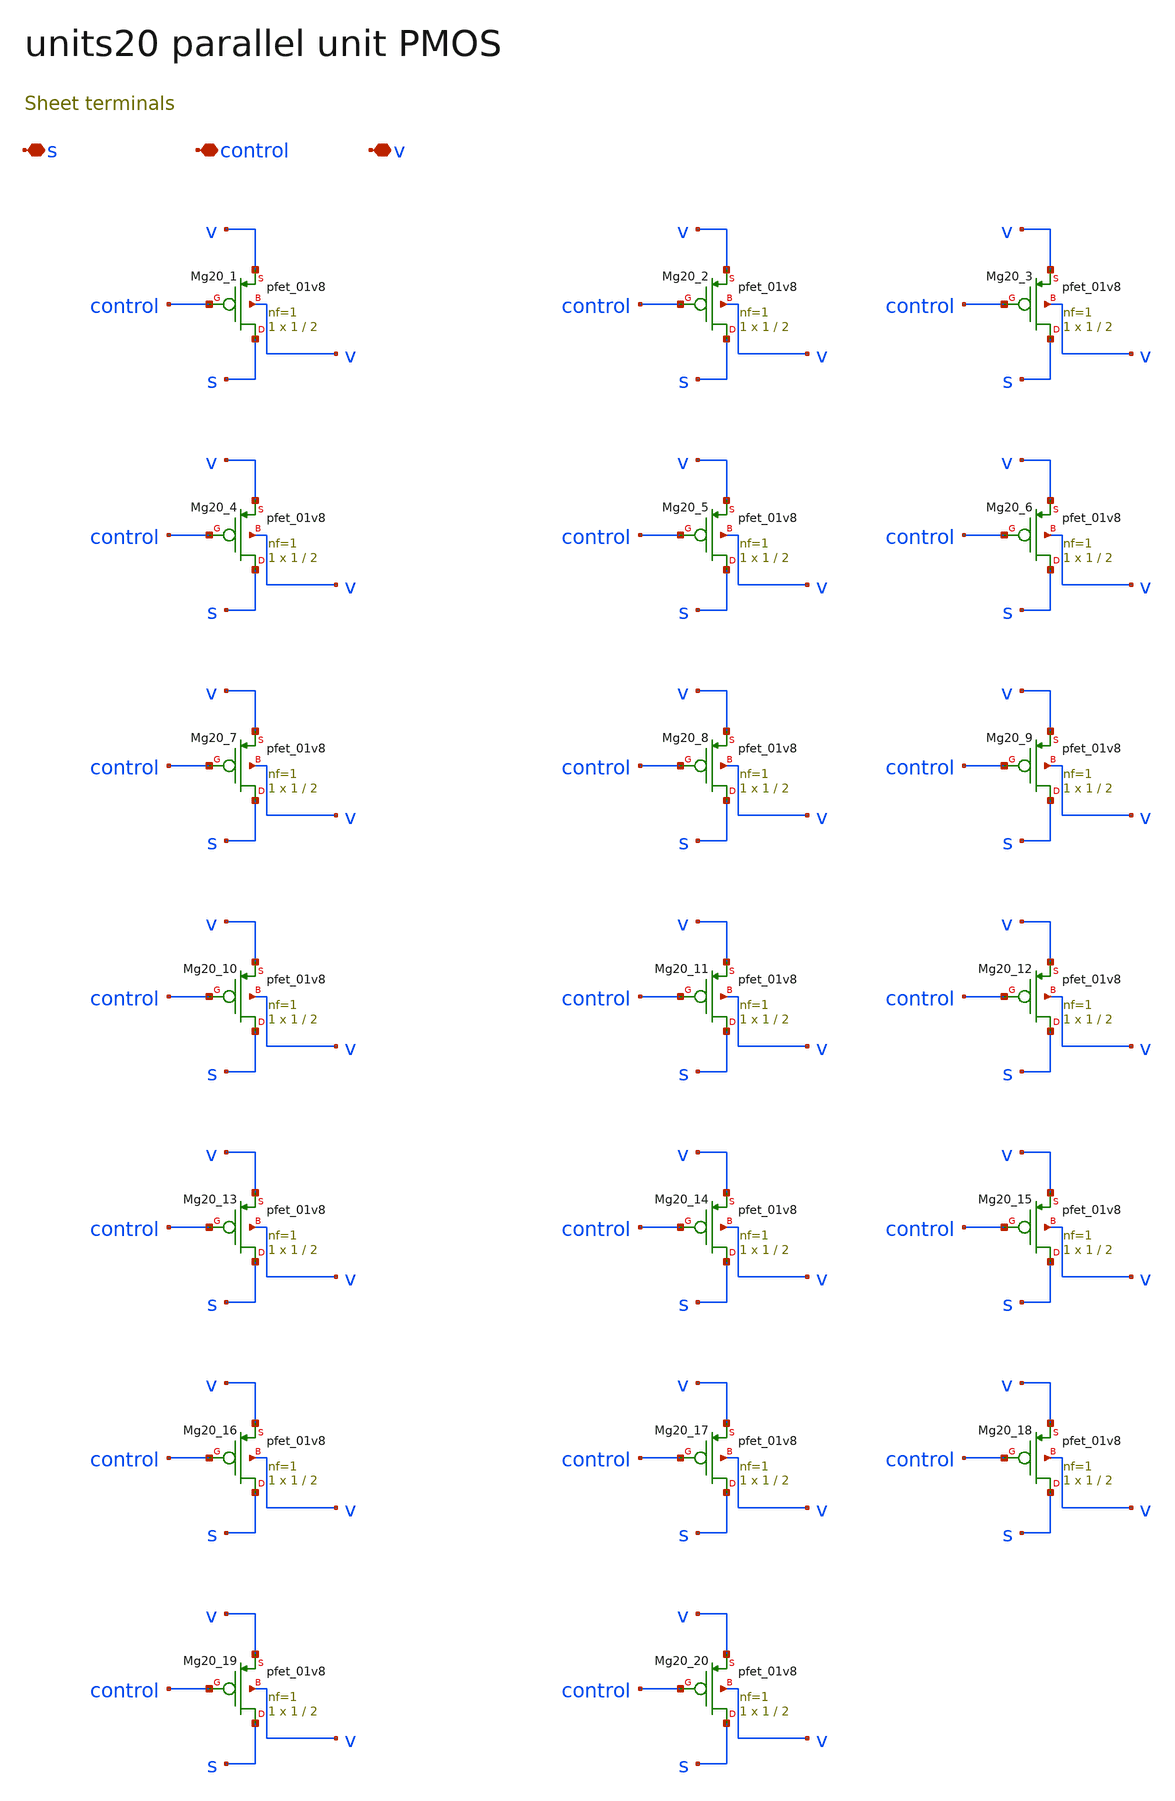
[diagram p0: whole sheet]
** sch_path: review/xschem/units20.sch
**.subckt units20 s control v
*.iopin s
*.iopin control
*.iopin v
XMg20_1 s control v v sky130_fd_pr__pfet_01v8 L=2 W=1 nf=1 ad='int((nf+1)/2) * W/nf * 0.29' as='int((nf+2)/2) * W/nf * 0.29'
+ pd='2*int((nf+1)/2) * (W/nf + 0.29)' ps='2*int((nf+2)/2) * (W/nf + 0.29)' nrd='0.29 / W' nrs='0.29 / W'
+ sa=0 sb=0 sd=0 mult=1 m=1
XMg20_2 s control v v sky130_fd_pr__pfet_01v8 L=2 W=1 nf=1 ad='int((nf+1)/2) * W/nf * 0.29' as='int((nf+2)/2) * W/nf * 0.29'
+ pd='2*int((nf+1)/2) * (W/nf + 0.29)' ps='2*int((nf+2)/2) * (W/nf + 0.29)' nrd='0.29 / W' nrs='0.29 / W'
+ sa=0 sb=0 sd=0 mult=1 m=1
XMg20_3 s control v v sky130_fd_pr__pfet_01v8 L=2 W=1 nf=1 ad='int((nf+1)/2) * W/nf * 0.29' as='int((nf+2)/2) * W/nf * 0.29'
+ pd='2*int((nf+1)/2) * (W/nf + 0.29)' ps='2*int((nf+2)/2) * (W/nf + 0.29)' nrd='0.29 / W' nrs='0.29 / W'
+ sa=0 sb=0 sd=0 mult=1 m=1
XMg20_4 s control v v sky130_fd_pr__pfet_01v8 L=2 W=1 nf=1 ad='int((nf+1)/2) * W/nf * 0.29' as='int((nf+2)/2) * W/nf * 0.29'
+ pd='2*int((nf+1)/2) * (W/nf + 0.29)' ps='2*int((nf+2)/2) * (W/nf + 0.29)' nrd='0.29 / W' nrs='0.29 / W'
+ sa=0 sb=0 sd=0 mult=1 m=1
XMg20_5 s control v v sky130_fd_pr__pfet_01v8 L=2 W=1 nf=1 ad='int((nf+1)/2) * W/nf * 0.29' as='int((nf+2)/2) * W/nf * 0.29'
+ pd='2*int((nf+1)/2) * (W/nf + 0.29)' ps='2*int((nf+2)/2) * (W/nf + 0.29)' nrd='0.29 / W' nrs='0.29 / W'
+ sa=0 sb=0 sd=0 mult=1 m=1
XMg20_6 s control v v sky130_fd_pr__pfet_01v8 L=2 W=1 nf=1 ad='int((nf+1)/2) * W/nf * 0.29' as='int((nf+2)/2) * W/nf * 0.29'
+ pd='2*int((nf+1)/2) * (W/nf + 0.29)' ps='2*int((nf+2)/2) * (W/nf + 0.29)' nrd='0.29 / W' nrs='0.29 / W'
+ sa=0 sb=0 sd=0 mult=1 m=1
XMg20_7 s control v v sky130_fd_pr__pfet_01v8 L=2 W=1 nf=1 ad='int((nf+1)/2) * W/nf * 0.29' as='int((nf+2)/2) * W/nf * 0.29'
+ pd='2*int((nf+1)/2) * (W/nf + 0.29)' ps='2*int((nf+2)/2) * (W/nf + 0.29)' nrd='0.29 / W' nrs='0.29 / W'
+ sa=0 sb=0 sd=0 mult=1 m=1
XMg20_8 s control v v sky130_fd_pr__pfet_01v8 L=2 W=1 nf=1 ad='int((nf+1)/2) * W/nf * 0.29' as='int((nf+2)/2) * W/nf * 0.29'
+ pd='2*int((nf+1)/2) * (W/nf + 0.29)' ps='2*int((nf+2)/2) * (W/nf + 0.29)' nrd='0.29 / W' nrs='0.29 / W'
+ sa=0 sb=0 sd=0 mult=1 m=1
XMg20_9 s control v v sky130_fd_pr__pfet_01v8 L=2 W=1 nf=1 ad='int((nf+1)/2) * W/nf * 0.29' as='int((nf+2)/2) * W/nf * 0.29'
+ pd='2*int((nf+1)/2) * (W/nf + 0.29)' ps='2*int((nf+2)/2) * (W/nf + 0.29)' nrd='0.29 / W' nrs='0.29 / W'
+ sa=0 sb=0 sd=0 mult=1 m=1
XMg20_10 s control v v sky130_fd_pr__pfet_01v8 L=2 W=1 nf=1 ad='int((nf+1)/2) * W/nf * 0.29' as='int((nf+2)/2) * W/nf * 0.29'
+ pd='2*int((nf+1)/2) * (W/nf + 0.29)' ps='2*int((nf+2)/2) * (W/nf + 0.29)' nrd='0.29 / W' nrs='0.29 / W'
+ sa=0 sb=0 sd=0 mult=1 m=1
XMg20_11 s control v v sky130_fd_pr__pfet_01v8 L=2 W=1 nf=1 ad='int((nf+1)/2) * W/nf * 0.29' as='int((nf+2)/2) * W/nf * 0.29'
+ pd='2*int((nf+1)/2) * (W/nf + 0.29)' ps='2*int((nf+2)/2) * (W/nf + 0.29)' nrd='0.29 / W' nrs='0.29 / W'
+ sa=0 sb=0 sd=0 mult=1 m=1
XMg20_12 s control v v sky130_fd_pr__pfet_01v8 L=2 W=1 nf=1 ad='int((nf+1)/2) * W/nf * 0.29' as='int((nf+2)/2) * W/nf * 0.29'
+ pd='2*int((nf+1)/2) * (W/nf + 0.29)' ps='2*int((nf+2)/2) * (W/nf + 0.29)' nrd='0.29 / W' nrs='0.29 / W'
+ sa=0 sb=0 sd=0 mult=1 m=1
XMg20_13 s control v v sky130_fd_pr__pfet_01v8 L=2 W=1 nf=1 ad='int((nf+1)/2) * W/nf * 0.29' as='int((nf+2)/2) * W/nf * 0.29'
+ pd='2*int((nf+1)/2) * (W/nf + 0.29)' ps='2*int((nf+2)/2) * (W/nf + 0.29)' nrd='0.29 / W' nrs='0.29 / W'
+ sa=0 sb=0 sd=0 mult=1 m=1
XMg20_14 s control v v sky130_fd_pr__pfet_01v8 L=2 W=1 nf=1 ad='int((nf+1)/2) * W/nf * 0.29' as='int((nf+2)/2) * W/nf * 0.29'
+ pd='2*int((nf+1)/2) * (W/nf + 0.29)' ps='2*int((nf+2)/2) * (W/nf + 0.29)' nrd='0.29 / W' nrs='0.29 / W'
+ sa=0 sb=0 sd=0 mult=1 m=1
XMg20_15 s control v v sky130_fd_pr__pfet_01v8 L=2 W=1 nf=1 ad='int((nf+1)/2) * W/nf * 0.29' as='int((nf+2)/2) * W/nf * 0.29'
+ pd='2*int((nf+1)/2) * (W/nf + 0.29)' ps='2*int((nf+2)/2) * (W/nf + 0.29)' nrd='0.29 / W' nrs='0.29 / W'
+ sa=0 sb=0 sd=0 mult=1 m=1
XMg20_16 s control v v sky130_fd_pr__pfet_01v8 L=2 W=1 nf=1 ad='int((nf+1)/2) * W/nf * 0.29' as='int((nf+2)/2) * W/nf * 0.29'
+ pd='2*int((nf+1)/2) * (W/nf + 0.29)' ps='2*int((nf+2)/2) * (W/nf + 0.29)' nrd='0.29 / W' nrs='0.29 / W'
+ sa=0 sb=0 sd=0 mult=1 m=1
XMg20_17 s control v v sky130_fd_pr__pfet_01v8 L=2 W=1 nf=1 ad='int((nf+1)/2) * W/nf * 0.29' as='int((nf+2)/2) * W/nf * 0.29'
+ pd='2*int((nf+1)/2) * (W/nf + 0.29)' ps='2*int((nf+2)/2) * (W/nf + 0.29)' nrd='0.29 / W' nrs='0.29 / W'
+ sa=0 sb=0 sd=0 mult=1 m=1
XMg20_18 s control v v sky130_fd_pr__pfet_01v8 L=2 W=1 nf=1 ad='int((nf+1)/2) * W/nf * 0.29' as='int((nf+2)/2) * W/nf * 0.29'
+ pd='2*int((nf+1)/2) * (W/nf + 0.29)' ps='2*int((nf+2)/2) * (W/nf + 0.29)' nrd='0.29 / W' nrs='0.29 / W'
+ sa=0 sb=0 sd=0 mult=1 m=1
XMg20_19 s control v v sky130_fd_pr__pfet_01v8 L=2 W=1 nf=1 ad='int((nf+1)/2) * W/nf * 0.29' as='int((nf+2)/2) * W/nf * 0.29'
+ pd='2*int((nf+1)/2) * (W/nf + 0.29)' ps='2*int((nf+2)/2) * (W/nf + 0.29)' nrd='0.29 / W' nrs='0.29 / W'
+ sa=0 sb=0 sd=0 mult=1 m=1
XMg20_20 s control v v sky130_fd_pr__pfet_01v8 L=2 W=1 nf=1 ad='int((nf+1)/2) * W/nf * 0.29' as='int((nf+2)/2) * W/nf * 0.29'
+ pd='2*int((nf+1)/2) * (W/nf + 0.29)' ps='2*int((nf+2)/2) * (W/nf + 0.29)' nrd='0.29 / W' nrs='0.29 / W'
+ sa=0 sb=0 sd=0 mult=1 m=1
**.ends
.end
